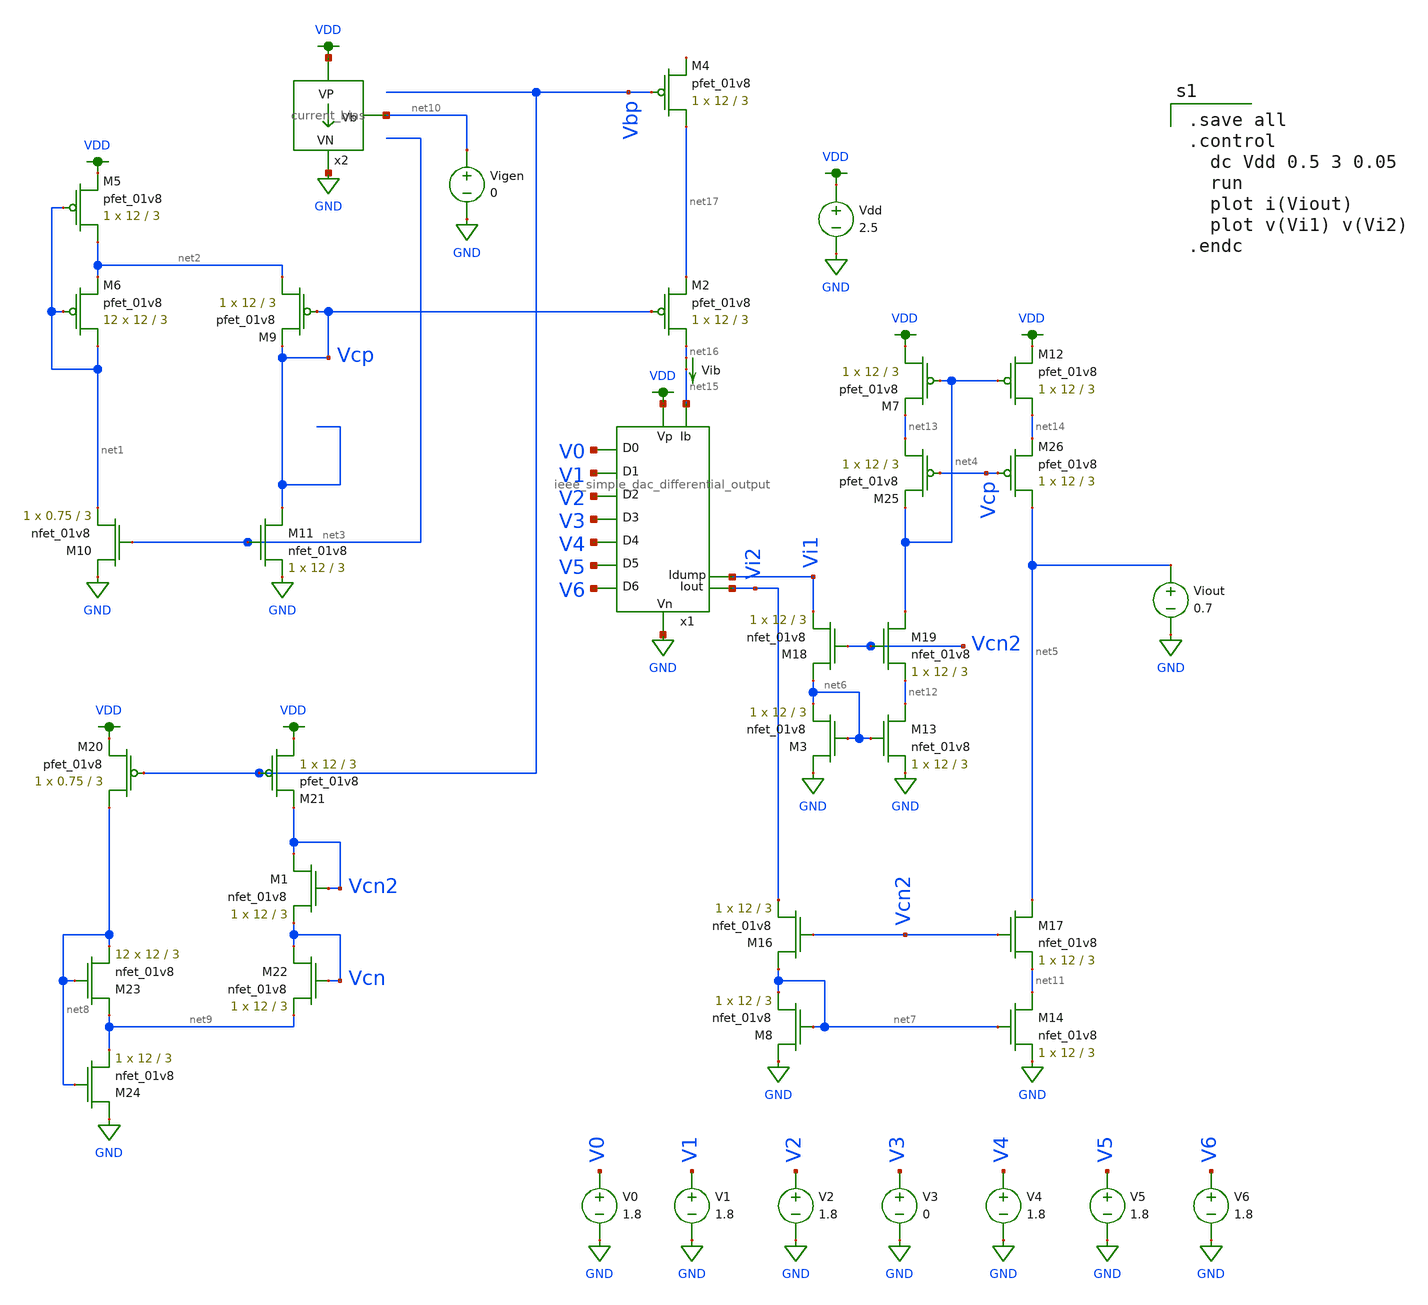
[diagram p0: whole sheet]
** sch_path: schematics/ieee DAC/ieee_DAC_mc_simulation_8.sch
**.subckt ieee_DAC_mc_simulation_8
Vdd VDD GND 2.5
V1 V1 GND 1.8
V2 V2 GND 1.8
V3 V3 GND 0
V4 V4 GND 1.8
V5 V5 GND 1.8
V6 V6 GND 1.8
V0 V0 GND 1.8
XM5 net2 net1 VDD VDD sky130_fd_pr__pfet_01v8 L=3 W=12 nf=1 ad='int((nf+1)/2) * W/nf * 0.29' as='int((nf+2)/2) * W/nf * 0.29'
+ pd='2*int((nf+1)/2) * (W/nf + 0.29)' ps='2*int((nf+2)/2) * (W/nf + 0.29)' nrd='0.29 / W' nrs='0.29 / W'
+ sa=0 sb=0 sd=0 mult=1 m=1
XM6 net1 net1 net2 VDD sky130_fd_pr__pfet_01v8 L=3 W=12 nf=1 ad='int((nf+1)/2) * W/nf * 0.29' as='int((nf+2)/2) * W/nf * 0.29'
+ pd='2*int((nf+1)/2) * (W/nf + 0.29)' ps='2*int((nf+2)/2) * (W/nf + 0.29)' nrd='0.29 / W' nrs='0.29 / W'
+ sa=0 sb=0 sd=0 mult=12 m=12
XM9 net2 Vcp Vcp VDD sky130_fd_pr__pfet_01v8 L=3 W=12 nf=1 ad='int((nf+1)/2) * W/nf * 0.29' as='int((nf+2)/2) * W/nf * 0.29'
+ pd='2*int((nf+1)/2) * (W/nf + 0.29)' ps='2*int((nf+2)/2) * (W/nf + 0.29)' nrd='0.29 / W' nrs='0.29 / W'
+ sa=0 sb=0 sd=0 mult=1 m=1
XM10 GND net3 net1 GND sky130_fd_pr__nfet_01v8 L=3 W=0.75 nf=1 ad='int((nf+1)/2) * W/nf * 0.29' as='int((nf+2)/2) * W/nf * 0.29'
+ pd='2*int((nf+1)/2) * (W/nf + 0.29)' ps='2*int((nf+2)/2) * (W/nf + 0.29)' nrd='0.29 / W' nrs='0.29 / W'
+ sa=0 sb=0 sd=0 mult=1 m=1
XM11 Vcp net3 GND GND sky130_fd_pr__nfet_01v8 L=3 W=12 nf=1 ad='int((nf+1)/2) * W/nf * 0.29' as='int((nf+2)/2) * W/nf * 0.29'
+ pd='2*int((nf+1)/2) * (W/nf + 0.29)' ps='2*int((nf+2)/2) * (W/nf + 0.29)' nrd='0.29 / W' nrs='0.29 / W'
+ sa=0 sb=0 sd=0 mult=1 m=1
x2 VDD net10 GND current_bias
Vigen net10 GND 0
XM3 GND net6 net6 GND sky130_fd_pr__nfet_01v8 L=3 W=12 nf=1 ad='int((nf+1)/2) * W/nf * 0.29' as='int((nf+2)/2) * W/nf * 0.29'
+ pd='2*int((nf+1)/2) * (W/nf + 0.29)' ps='2*int((nf+2)/2) * (W/nf + 0.29)' nrd='0.29 / W' nrs='0.29 / W'
+ sa=0 sb=0 sd=0 mult=1 m=1
XM7 VDD net4 net13 VDD sky130_fd_pr__pfet_01v8 L=3 W=12 nf=1 ad='int((nf+1)/2) * W/nf * 0.29' as='int((nf+2)/2) * W/nf * 0.29'
+ pd='2*int((nf+1)/2) * (W/nf + 0.29)' ps='2*int((nf+2)/2) * (W/nf + 0.29)' nrd='0.29 / W' nrs='0.29 / W'
+ sa=0 sb=0 sd=0 mult=1 m=1
XM8 GND net7 net7 GND sky130_fd_pr__nfet_01v8 L=3 W=12 nf=1 ad='int((nf+1)/2) * W/nf * 0.29' as='int((nf+2)/2) * W/nf * 0.29'
+ pd='2*int((nf+1)/2) * (W/nf + 0.29)' ps='2*int((nf+2)/2) * (W/nf + 0.29)' nrd='0.29 / W' nrs='0.29 / W'
+ sa=0 sb=0 sd=0 mult=1 m=1
XM12 net14 net4 VDD VDD sky130_fd_pr__pfet_01v8 L=3 W=12 nf=1 ad='int((nf+1)/2) * W/nf * 0.29' as='int((nf+2)/2) * W/nf * 0.29'
+ pd='2*int((nf+1)/2) * (W/nf + 0.29)' ps='2*int((nf+2)/2) * (W/nf + 0.29)' nrd='0.29 / W' nrs='0.29 / W'
+ sa=0 sb=0 sd=0 mult=1 m=1
Viout net5 GND 0.7
XM13 net12 net6 GND GND sky130_fd_pr__nfet_01v8 L=3 W=12 nf=1 ad='int((nf+1)/2) * W/nf * 0.29' as='int((nf+2)/2) * W/nf * 0.29'
+ pd='2*int((nf+1)/2) * (W/nf + 0.29)' ps='2*int((nf+2)/2) * (W/nf + 0.29)' nrd='0.29 / W' nrs='0.29 / W'
+ sa=0 sb=0 sd=0 mult=1 m=1
XM14 net11 net7 GND GND sky130_fd_pr__nfet_01v8 L=3 W=12 nf=1 ad='int((nf+1)/2) * W/nf * 0.29' as='int((nf+2)/2) * W/nf * 0.29'
+ pd='2*int((nf+1)/2) * (W/nf + 0.29)' ps='2*int((nf+2)/2) * (W/nf + 0.29)' nrd='0.29 / W' nrs='0.29 / W'
+ sa=0 sb=0 sd=0 mult=1 m=1
XM20 net8 Vbp VDD VDD sky130_fd_pr__pfet_01v8 L=3 W=0.75 nf=1 ad='int((nf+1)/2) * W/nf * 0.29' as='int((nf+2)/2) * W/nf * 0.29'
+ pd='2*int((nf+1)/2) * (W/nf + 0.29)' ps='2*int((nf+2)/2) * (W/nf + 0.29)' nrd='0.29 / W' nrs='0.29 / W'
+ sa=0 sb=0 sd=0 mult=1 m=1
XM21 VDD Vbp Vcn2 VDD sky130_fd_pr__pfet_01v8 L=3 W=12 nf=1 ad='int((nf+1)/2) * W/nf * 0.29' as='int((nf+2)/2) * W/nf * 0.29'
+ pd='2*int((nf+1)/2) * (W/nf + 0.29)' ps='2*int((nf+2)/2) * (W/nf + 0.29)' nrd='0.29 / W' nrs='0.29 / W'
+ sa=0 sb=0 sd=0 mult=1 m=1
XM22 Vcn Vcn net9 GND sky130_fd_pr__nfet_01v8 L=3 W=12 nf=1 ad='int((nf+1)/2) * W/nf * 0.29' as='int((nf+2)/2) * W/nf * 0.29'
+ pd='2*int((nf+1)/2) * (W/nf + 0.29)' ps='2*int((nf+2)/2) * (W/nf + 0.29)' nrd='0.29 / W' nrs='0.29 / W'
+ sa=0 sb=0 sd=0 mult=1 m=1
XM23 net9 net8 net8 GND sky130_fd_pr__nfet_01v8 L=3 W=12 nf=1 ad='int((nf+1)/2) * W/nf * 0.29' as='int((nf+2)/2) * W/nf * 0.29'
+ pd='2*int((nf+1)/2) * (W/nf + 0.29)' ps='2*int((nf+2)/2) * (W/nf + 0.29)' nrd='0.29 / W' nrs='0.29 / W'
+ sa=0 sb=0 sd=0 mult=12 m=12
XM24 GND net8 net9 GND sky130_fd_pr__nfet_01v8 L=3 W=12 nf=1 ad='int((nf+1)/2) * W/nf * 0.29' as='int((nf+2)/2) * W/nf * 0.29'
+ pd='2*int((nf+1)/2) * (W/nf + 0.29)' ps='2*int((nf+2)/2) * (W/nf + 0.29)' nrd='0.29 / W' nrs='0.29 / W'
+ sa=0 sb=0 sd=0 mult=1 m=1
XM16 net7 Vcn2 Vi2 GND sky130_fd_pr__nfet_01v8 L=3 W=12 nf=1 ad='int((nf+1)/2) * W/nf * 0.29' as='int((nf+2)/2) * W/nf * 0.29'
+ pd='2*int((nf+1)/2) * (W/nf + 0.29)' ps='2*int((nf+2)/2) * (W/nf + 0.29)' nrd='0.29 / W' nrs='0.29 / W'
+ sa=0 sb=0 sd=0 mult=1 m=1
XM17 net5 Vcn2 net11 GND sky130_fd_pr__nfet_01v8 L=3 W=12 nf=1 ad='int((nf+1)/2) * W/nf * 0.29' as='int((nf+2)/2) * W/nf * 0.29'
+ pd='2*int((nf+1)/2) * (W/nf + 0.29)' ps='2*int((nf+2)/2) * (W/nf + 0.29)' nrd='0.29 / W' nrs='0.29 / W'
+ sa=0 sb=0 sd=0 mult=1 m=1
XM18 net6 Vcn2 Vi1 GND sky130_fd_pr__nfet_01v8 L=3 W=12 nf=1 ad='int((nf+1)/2) * W/nf * 0.29' as='int((nf+2)/2) * W/nf * 0.29'
+ pd='2*int((nf+1)/2) * (W/nf + 0.29)' ps='2*int((nf+2)/2) * (W/nf + 0.29)' nrd='0.29 / W' nrs='0.29 / W'
+ sa=0 sb=0 sd=0 mult=1 m=1
XM19 net4 Vcn2 net12 GND sky130_fd_pr__nfet_01v8 L=3 W=12 nf=1 ad='int((nf+1)/2) * W/nf * 0.29' as='int((nf+2)/2) * W/nf * 0.29'
+ pd='2*int((nf+1)/2) * (W/nf + 0.29)' ps='2*int((nf+2)/2) * (W/nf + 0.29)' nrd='0.29 / W' nrs='0.29 / W'
+ sa=0 sb=0 sd=0 mult=1 m=1
XM25 net13 Vcp net4 VDD sky130_fd_pr__pfet_01v8 L=3 W=12 nf=1 ad='int((nf+1)/2) * W/nf * 0.29' as='int((nf+2)/2) * W/nf * 0.29'
+ pd='2*int((nf+1)/2) * (W/nf + 0.29)' ps='2*int((nf+2)/2) * (W/nf + 0.29)' nrd='0.29 / W' nrs='0.29 / W'
+ sa=0 sb=0 sd=0 mult=1 m=1
XM26 net5 Vcp net14 VDD sky130_fd_pr__pfet_01v8 L=3 W=12 nf=1 ad='int((nf+1)/2) * W/nf * 0.29' as='int((nf+2)/2) * W/nf * 0.29'
+ pd='2*int((nf+1)/2) * (W/nf + 0.29)' ps='2*int((nf+2)/2) * (W/nf + 0.29)' nrd='0.29 / W' nrs='0.29 / W'
+ sa=0 sb=0 sd=0 mult=1 m=1
XM1 Vcn2 Vcn2 Vcn GND sky130_fd_pr__nfet_01v8 L=3 W=12 nf=1 ad='int((nf+1)/2) * W/nf * 0.29' as='int((nf+2)/2) * W/nf * 0.29'
+ pd='2*int((nf+1)/2) * (W/nf + 0.29)' ps='2*int((nf+2)/2) * (W/nf + 0.29)' nrd='0.29 / W' nrs='0.29 / W'
+ sa=0 sb=0 sd=0 mult=1 m=1
x1 VDD Vi1 GND V1 V0 V2 V3 V4 V5 V6 net15 Vi2 ieee_simple_dac_differential_output
Vib net16 net15 0
.save i(vib)
XM2 net16 Vcp net17 VDD sky130_fd_pr__pfet_01v8 L=3 W=12 nf=1 ad='int((nf+1)/2) * W/nf * 0.29' as='int((nf+2)/2) * W/nf * 0.29'
+ pd='2*int((nf+1)/2) * (W/nf + 0.29)' ps='2*int((nf+2)/2) * (W/nf + 0.29)' nrd='0.29 / W' nrs='0.29 / W'
+ sa=0 sb=0 sd=0 mult=1 m=1
XM4 net17 Vbp net18 VDD sky130_fd_pr__pfet_01v8 L=3 W=12 nf=1 ad='int((nf+1)/2) * W/nf * 0.29' as='int((nf+2)/2) * W/nf * 0.29'
+ pd='2*int((nf+1)/2) * (W/nf + 0.29)' ps='2*int((nf+2)/2) * (W/nf + 0.29)' nrd='0.29 / W' nrs='0.29 / W'
+ sa=0 sb=0 sd=0 mult=1 m=1
**** begin user architecture code

.option wnflag=1
.param MC_SWITCH=1.0
.lib ~/skywater/skywater-pdk/libraries/sky130_fd_pr_ngspice/latest/models/sky130.lib.spice tt


.save all
.control
  dc Vdd 0.5 3 0.05
  run
  plot i(Viout)
  plot v(Vi1) v(Vi2)
.endc

**** end user architecture code
**.ends
.GLOBAL GND
.GLOBAL VDD
.end
